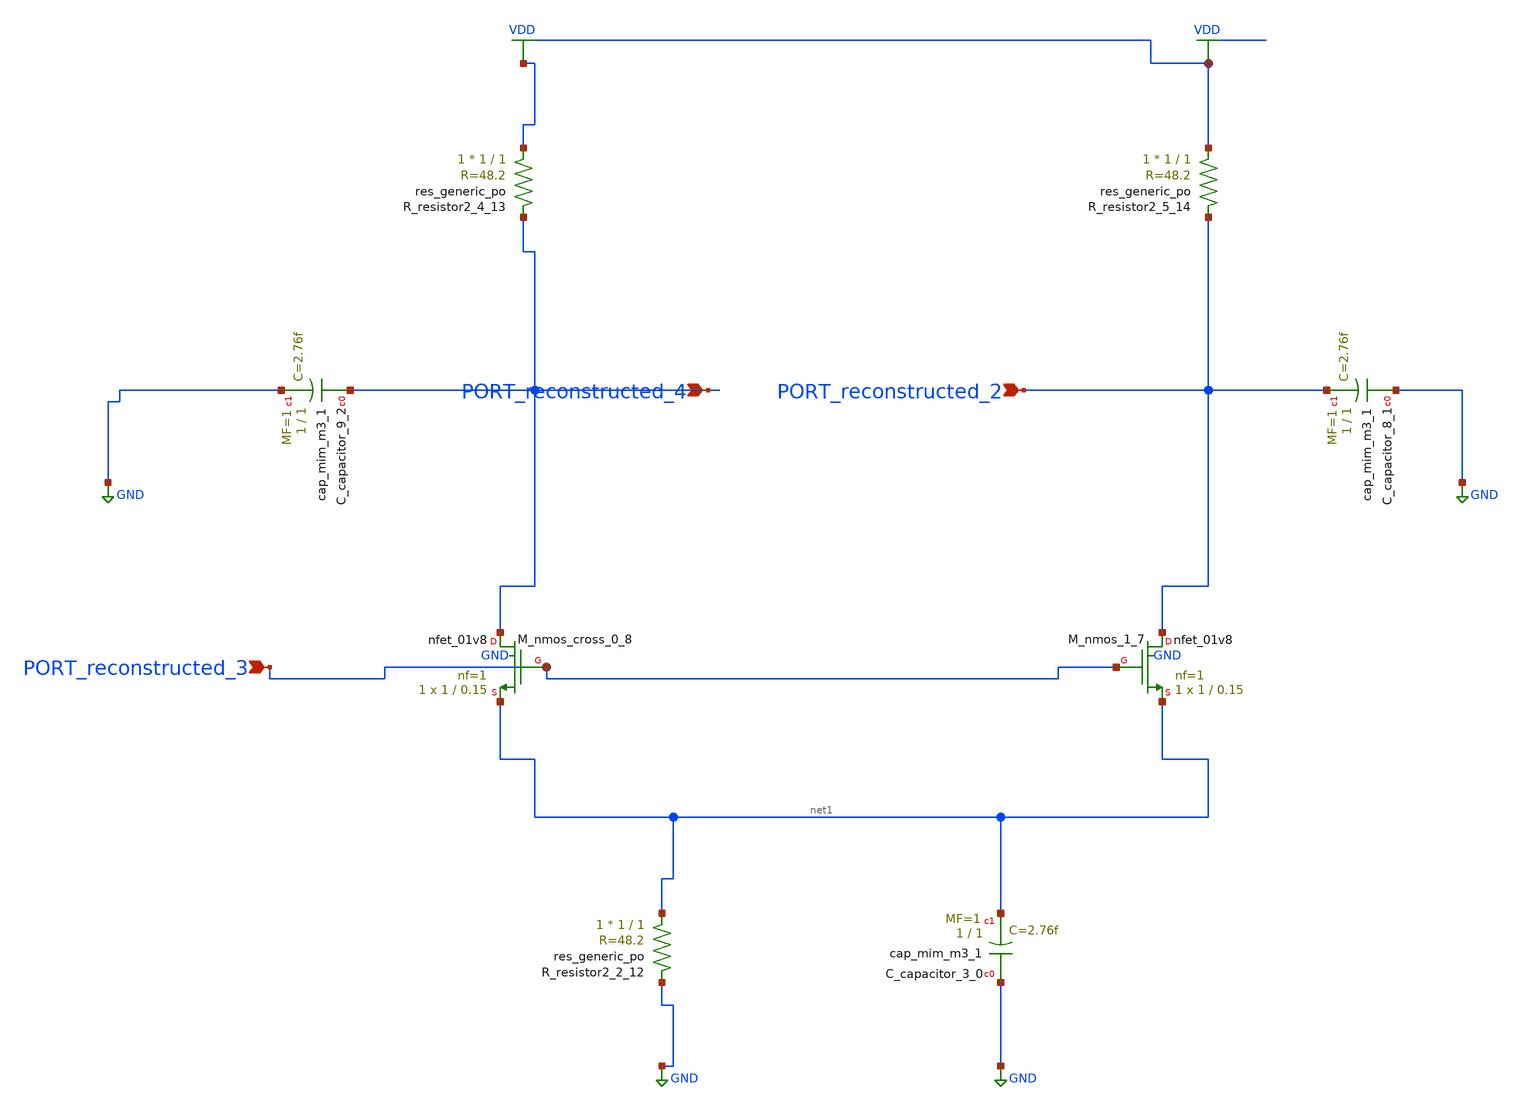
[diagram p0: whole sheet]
** sch_path: schematics/AMSNet/386.sch
**.subckt 386 PORT_reconstructed_2 PORT_reconstructed_4 PORT_reconstructed_3
*.ipin PORT_reconstructed_2
*.ipin PORT_reconstructed_4
*.ipin PORT_reconstructed_3
XC_capacitor_3_0 GND net1 sky130_fd_pr__cap_mim_m3_1 W=1 L=1 MF=1 m=1
XC_capacitor_8_1 GND PORT_reconstructed_2 sky130_fd_pr__cap_mim_m3_1 W=1 L=1 MF=1 m=1
XC_capacitor_9_2 PORT_reconstructed_4 GND sky130_fd_pr__cap_mim_m3_1 W=1 L=1 MF=1 m=1
XM_nmos_1_7 PORT_reconstructed_2 PORT_reconstructed_3 net1 GND sky130_fd_pr__nfet_01v8 L=0.15 W=1 nf=1
+ ad='int((1 + 1)/2) * 1 / 1 * 0.29' as='int((1 + 2)/2) * 1 / 1 * 0.29' pd='2*int((1 + 1)/2) * (1 / 1 + 0.29)'
+ ps='2*int((1 + 2)/2) * (1 / 1 + 0.29)' nrd='0.29 / 1 ' nrs='0.29 / 1 ' sa=0 sb=0 sd=0 mult=1 m=1
XM_nmos_cross_0_8 PORT_reconstructed_4 PORT_reconstructed_3 net1 GND sky130_fd_pr__nfet_01v8 L=0.15 W=1
+ nf=1 ad='int((1 + 1)/2) * 1 / 1 * 0.29' as='int((1 + 2)/2) * 1 / 1 * 0.29' pd='2*int((1 + 1)/2) * (1 / 1 + 0.29)'
+ ps='2*int((1 + 2)/2) * (1 / 1 + 0.29)' nrd='0.29 / 1 ' nrs='0.29 / 1 ' sa=0 sb=0 sd=0 mult=1 m=1
XR_resistor2_2_12 net1 GND sky130_fd_pr__res_generic_po W=1 L=1 m=1
XR_resistor2_4_13 VDD PORT_reconstructed_4 sky130_fd_pr__res_generic_po W=1 L=1 m=1
XR_resistor2_5_14 VDD PORT_reconstructed_2 sky130_fd_pr__res_generic_po W=1 L=1 m=1
**.ends
.GLOBAL GND
.GLOBAL VDD
.end
